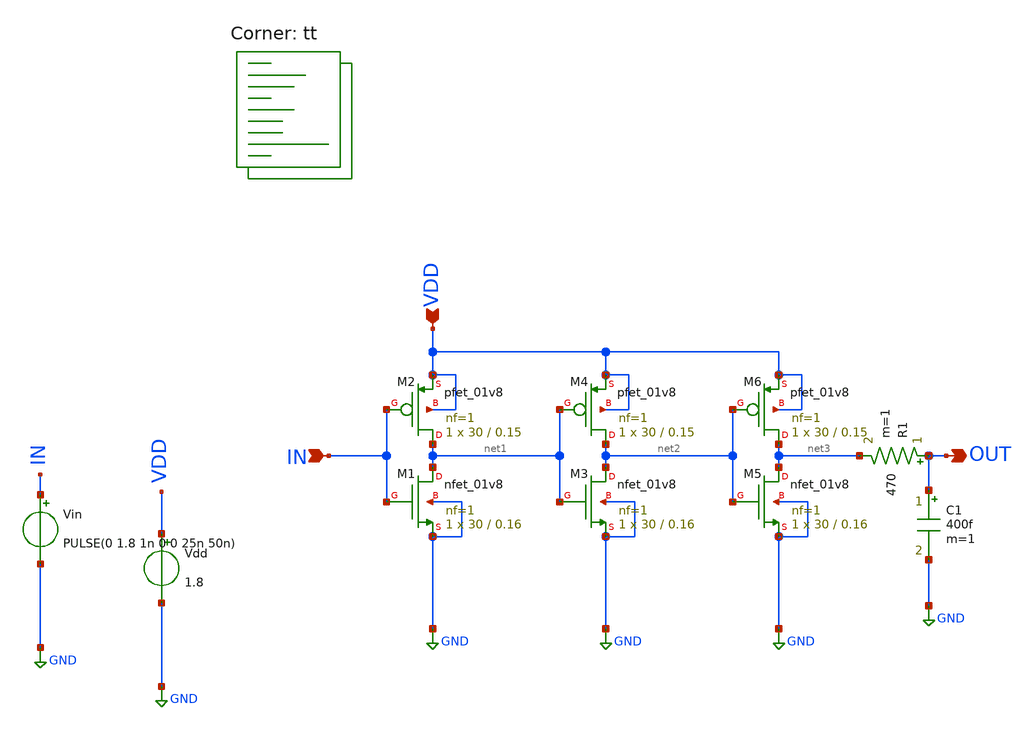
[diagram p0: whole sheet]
** sch_path: sizing-inverter.sch
**.subckt sizing-inverter IN VDD OUT
*.ipin IN
*.ipin VDD
*.opin OUT
Vin IN GND PULSE(0 1.8 1n 0 0 25n 50n)
Vdd VDD GND 1.8
XM1 net1 IN GND GND sky130_fd_pr__nfet_01v8 L=0.16 W=30 nf=1 ad='int((nf+1)/2) * W/nf * 0.29' as='int((nf+2)/2) * W/nf * 0.29'
+ pd='2*int((nf+1)/2) * (W/nf + 0.29)' ps='2*int((nf+2)/2) * (W/nf + 0.29)' nrd='0.29 / W' nrs='0.29 / W'
+ sa=0 sb=0 sd=0 mult=1 m=1
XM2 net1 IN VDD VDD sky130_fd_pr__pfet_01v8 L=0.15 W=30 nf=1 ad='int((nf+1)/2) * W/nf * 0.29' as='int((nf+2)/2) * W/nf * 0.29'
+ pd='2*int((nf+1)/2) * (W/nf + 0.29)' ps='2*int((nf+2)/2) * (W/nf + 0.29)' nrd='0.29 / W' nrs='0.29 / W'
+ sa=0 sb=0 sd=0 mult=1 m=1
C1 OUT GND 400f m=1
R1 OUT net3 470 m=1
XM3 net2 net1 GND GND sky130_fd_pr__nfet_01v8 L=0.16 W=30 nf=1 ad='int((nf+1)/2) * W/nf * 0.29' as='int((nf+2)/2) * W/nf * 0.29'
+ pd='2*int((nf+1)/2) * (W/nf + 0.29)' ps='2*int((nf+2)/2) * (W/nf + 0.29)' nrd='0.29 / W' nrs='0.29 / W'
+ sa=0 sb=0 sd=0 mult=1 m=1
XM4 net2 net1 VDD VDD sky130_fd_pr__pfet_01v8 L=0.15 W=30 nf=1 ad='int((nf+1)/2) * W/nf * 0.29' as='int((nf+2)/2) * W/nf * 0.29'
+ pd='2*int((nf+1)/2) * (W/nf + 0.29)' ps='2*int((nf+2)/2) * (W/nf + 0.29)' nrd='0.29 / W' nrs='0.29 / W'
+ sa=0 sb=0 sd=0 mult=1 m=1
XM5 net3 net2 GND GND sky130_fd_pr__nfet_01v8 L=0.16 W=30 nf=1 ad='int((nf+1)/2) * W/nf * 0.29' as='int((nf+2)/2) * W/nf * 0.29'
+ pd='2*int((nf+1)/2) * (W/nf + 0.29)' ps='2*int((nf+2)/2) * (W/nf + 0.29)' nrd='0.29 / W' nrs='0.29 / W'
+ sa=0 sb=0 sd=0 mult=1 m=1
XM6 net3 net2 VDD VDD sky130_fd_pr__pfet_01v8 L=0.15 W=30 nf=1 ad='int((nf+1)/2) * W/nf * 0.29' as='int((nf+2)/2) * W/nf * 0.29'
+ pd='2*int((nf+1)/2) * (W/nf + 0.29)' ps='2*int((nf+2)/2) * (W/nf + 0.29)' nrd='0.29 / W' nrs='0.29 / W'
+ sa=0 sb=0 sd=0 mult=1 m=1
**** begin user architecture code
.lib $::SKYWATER_MODELS/sky130.lib.spice tt


.options savecurrents

.control
save all

setplot const
let nmos_index = 0
let nmos_w = 0.5
let nmos_final = 20
let nmos_step = 1

let nmos_length = ceil((nmos_final - nmos_w)/nmos_step)

let pmos_initial = 1
let pmos_w = pmos_initial
let pmos_final = 40
let pmos_step = 1

let switching_points = vector(nmos_length)
let asymmetricity = vector(nmos_length)
let Rdon_pmos = vector(nmos_length)
let Rdon_nmos = vector(nmos_length)
let rise_times = vector(nmos_length)
let fall_times = vector(nmos_length)
let pmos_width = vector(nmos_length)
let nmos_width = vector(nmos_length)

set tranplots = ' '
set swplots = ' '

while nmos_w < nmos_final

  alter m.xm1.msky130_fd_pr__nfet_01v8 W = nmos_w
  alter m.xm3.msky130_fd_pr__nfet_01v8 W = e *nmos_w
  alter m.xm5.msky130_fd_pr__nfet_01v8 W = e * e * nmos_w


  let minimum_asym = 100
  let minimum_width_pmos = 100

  let pmos_w = pmos_initial

**** Find least asymmetric pmos_w ****
  while pmos_w < pmos_final

    alter m.xm2.msky130_fd_pr__pfet_01v8 W = pmos_w
    alter m.xm4.msky130_fd_pr__pfet_01v8 W = e * pmos_w
    alter m.xm4.msky130_fd_pr__pfet_01v8 W = e * e * pmos_w

* Run transient analysis using a symmetric pulse of period 25n
    tran 10p 40n

    meas tran rise_time TRIG v(out) VAL=0.1 RISE=LAST TARG v(out) VAL=1.62 RISE=LAST
    meas tran fall_time TRIG v(out) VAL=1.62 FALL=1 TARG v(out) VAL=0.1 FALL=1
* Create array of diffs
    let diff = abs( $&rise_time - $&fall_time )

    if diff < minimum_asym
      let minimum_asym = diff
      let minimum_width_pmos = pmos_w
    end
    print diff minimum_asym minimum_width_pmos pmos_w
    print nmos_w pmos_w
    let pmos_w = pmos_w + pmos_step
  end

  alter m.xm2.msky130_fd_pr__pfet_01v8 W = minimum_width_pmos
  alter m.xm4.msky130_fd_pr__pfet_01v8 W = e *minimum_width_pmos
  alter m.xm6.msky130_fd_pr__pfet_01v8 W = e * e * minimum_width_pmos


**** Run trainsient again to get rise fall time ****
  tran 10p 40n
*** Second rise because transient artifacts are technically rises and falls
  meas tran tau_rise TRIG v(out) VAL=0 RISE=LAST TARG v(out) VAL=1.376 RISE=LAST
  meas tran tau_fall TRIG v(out) VAL=1.8 FALL=1 TARG v(out) VAL=0.6624 FALL=1


  let Rdon_nmos[nmos_index] = tau_fall/200f
  let Rdon_pmos[nmos_index] = tau_rise/200f
  let fall_times[nmos_index] = tau_fall * 5
  let rise_times[nmos_index] = tau_rise * 5

  set tranplots = ( $tranplots {$curplot}.v(out) )

**** Find switching point for aforementioned pmos_w ****

  dc vin 0 1.8 1m

  meas dc switching_point WHEN v(out)=v(in) CROSS=1

  let switching_points[nmos_index] = $&switching_point
  let pmos_width[nmos_index] = minimum_width_pmos
  let nmos_width[nmos_index] = nmos_w
  let asymmetricity[nmos_index] = minimum_asym
  print nmos_index minimum_width_pmos

  set swplots = ( $swplots {$curplot}.v(out) )


  let nmos_w = nmos_w + nmos_step
  let nmos_index = nmos_index + 1
end

set swplots = ( $swplots {$curplot}.v(in) )

set color2=red
set color3=blue

plot switching_points vs nmos_width xlabel 'W_n' ylabel 'Switching point' title 'Switching points vs width'
+ pointplot
plot pmos_width vs nmos_width xlabel 'W_n' ylabel 'Least asym W_p' title 'Optimal pmos width per nmos width'
+ pointplot
plot asymmetricity vs nmos_width  xlabel 'W_n' ylabel 'Least asym' title 'Least asymmetricity per nmos width'
+ pointplot
plot Rdon_pmos Rdon_nmos vs nmos_width xlabel 'W_n' ylabel 'R_don' title 'Rdon_nmos and pmos per nmos width'
+ pointplot
plot rise_times fall_times vs nmos_width

set nolegend

plot $swplots xlimit 800m 1 title 'Switching point envelope'
plot $tranplots xlimit 1n 3n title 'Transient fall envelope'
plot $tranplots xlimit 26n 28n title 'Transient rise envelope'


.endc


**** end user architecture code
**.ends
.GLOBAL GND
.end
